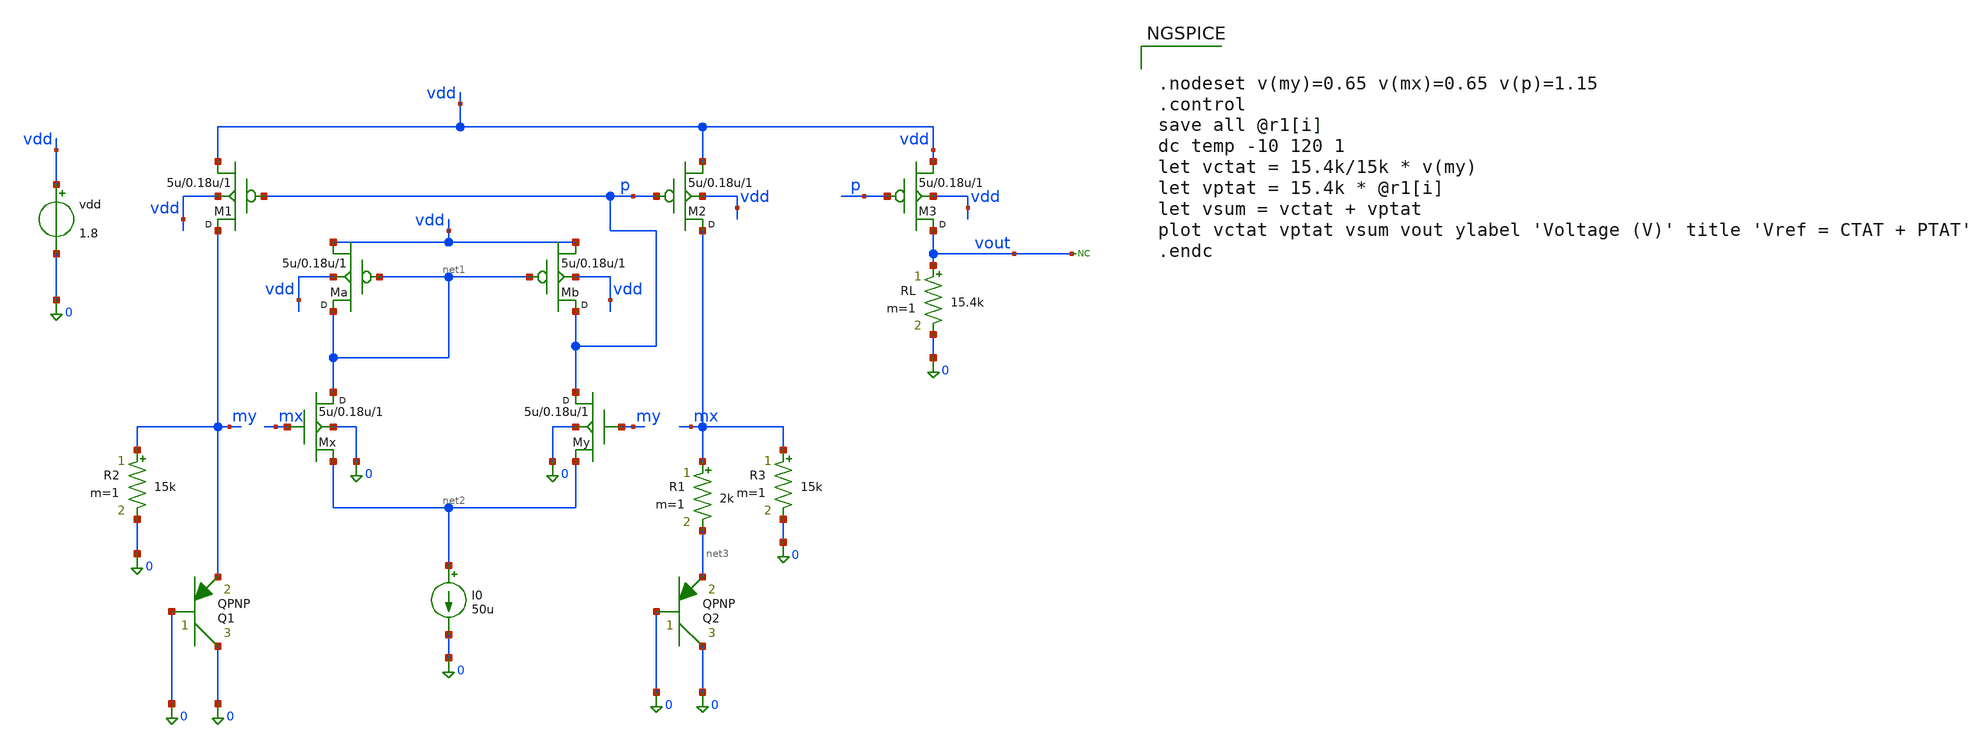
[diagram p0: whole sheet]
** sch_path: Schematic & Spice Files/BGR_Ideal.sch
**.subckt BGR_Ideal
I0 net2 0 50u
Q1 0 0 my QPNP area=4 m=1
Q2 0 0 net3 QPNP area=64 m=1
R1 mx net3 2k m=1
vdd vdd 0 1.8
R2 my 0 15k m=1
R3 mx 0 15k m=1
RL vout 0 15.4k m=1
* noconn vout
M1 my p vdd vdd PMOS1 w=5u l=0.18u m=1
M3 vout p vdd vdd PMOS1 w=5u l=0.18u m=1
Ma net1 net1 vdd vdd PMOS1 w=5u l=0.18u m=1
Mb p net1 vdd vdd PMOS1 w=5u l=0.18u m=1
Mx net1 mx net2 0 NMOS1 w=5u l=0.18u m=1
My p my net2 0 NMOS1 w=5u l=0.18u m=1
M2 mx p vdd vdd PMOS1 w=5u l=0.18u m=1
**** begin user architecture code


.model NMOS1 NMOS LEVEL=1 VTO=0.45 KP=200u LAMBDA=0.02
.model PMOS1 PMOS LEVEL=1 VTO=-0.45 KP=80u LAMBDA=0.02
.model QPNP PNP (IS=1e-16 BF=50 VAF=50)




.nodeset v(my)=0.65 v(mx)=0.65 v(p)=1.15
.control
save all @r1[i]
dc temp -10 120 1
let vctat = 15.4k/15k * v(my)
let vptat = 15.4k * @r1[i]
let vsum = vctat + vptat
plot vctat vptat vsum vout ylabel 'Voltage (V)' title 'Vref = CTAT + PTAT'
.endc

**** end user architecture code
**.ends
.end
